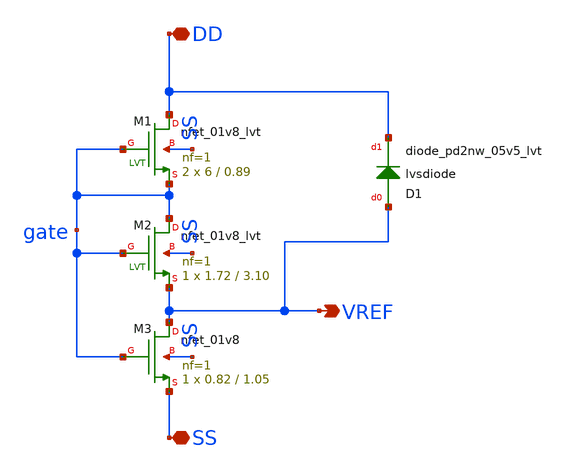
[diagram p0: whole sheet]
** sch_path: xschem/vref01_diode.sch
**.subckt vref01_diode VREF SS DD
*.opin VREF
*.iopin SS
*.iopin DD
XM1 DD gate gate SS sky130_fd_pr__nfet_01v8_lvt L=0.89 W=6 nf=1 ad='int((nf+1)/2) * W/nf * 0.29' as='int((nf+2)/2) * W/nf * 0.29'
+ pd='2*int((nf+1)/2) * (W/nf + 0.29)' ps='2*int((nf+2)/2) * (W/nf + 0.29)' nrd='0.29 / W' nrs='0.29 / W'
+ sa=0 sb=0 sd=0 mult=2 m=2
XM2 gate gate VREF SS sky130_fd_pr__nfet_01v8_lvt L=3.10 W=1.72 nf=1 ad='int((nf+1)/2) * W/nf * 0.29'
+ as='int((nf+2)/2) * W/nf * 0.29' pd='2*int((nf+1)/2) * (W/nf + 0.29)' ps='2*int((nf+2)/2) * (W/nf + 0.29)'
+ nrd='0.29 / W' nrs='0.29 / W' sa=0 sb=0 sd=0 mult=1 m=1
XM3 VREF gate SS SS sky130_fd_pr__nfet_01v8 L=1.05 W=0.82 nf=1 ad='int((nf+1)/2) * W/nf * 0.29' as='int((nf+2)/2) * W/nf * 0.29'
+ pd='2*int((nf+1)/2) * (W/nf + 0.29)' ps='2*int((nf+2)/2) * (W/nf + 0.29)' nrd='0.29 / W' nrs='0.29 / W'
+ sa=0 sb=0 sd=0 mult=1 m=1
D1 VREF DD sky130_fd_pr__diode_pd2nw_05v5_lvt area=4.225e+11
**.ends
.end
